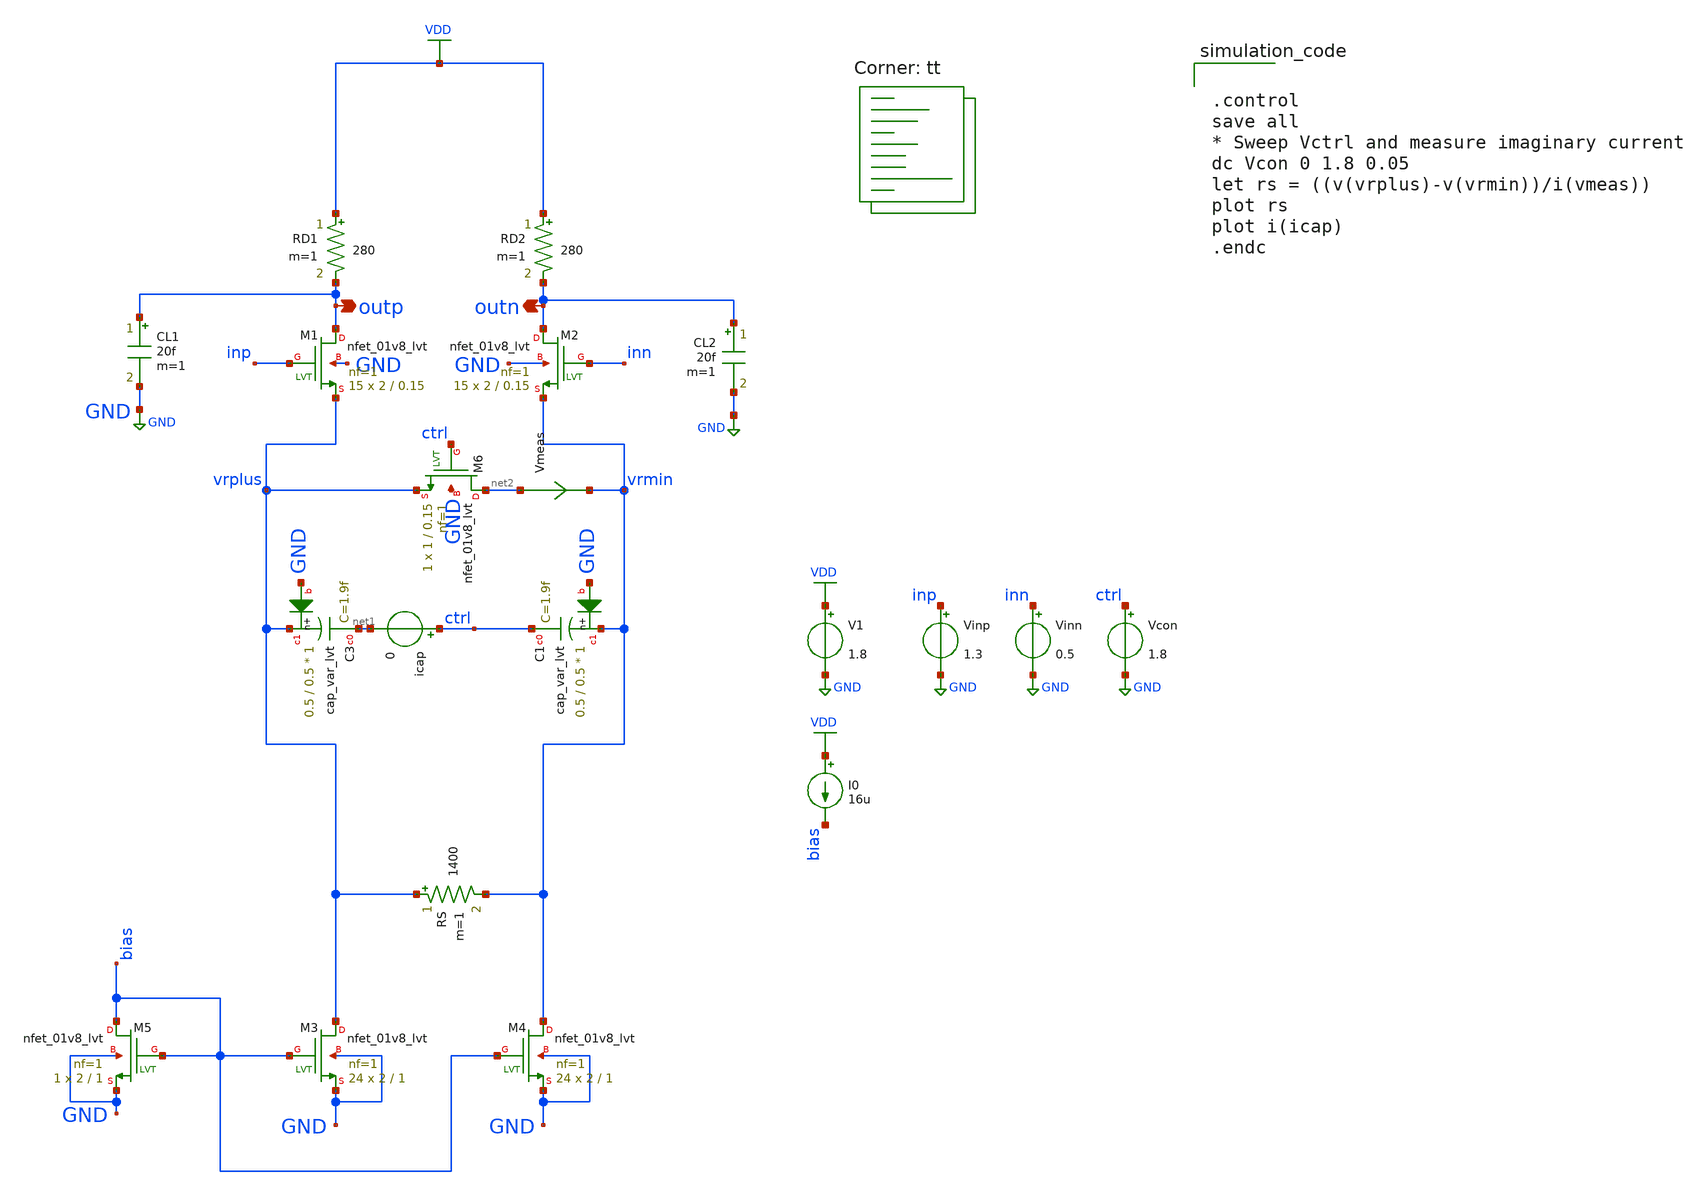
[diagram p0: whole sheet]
** sch_path: CTLE/ctle_sym_adaptive_cap.sch
**.subckt ctle_sym_adaptive_cap outp outn
*.opin outp
*.opin outn
XM1 outp inp vrplus GND sky130_fd_pr__nfet_01v8_lvt L=0.15 W=2 nf=1 ad='int((nf+1)/2) * W/nf * 0.29'
+ as='int((nf+2)/2) * W/nf * 0.29' pd='2*int((nf+1)/2) * (W/nf + 0.29)' ps='2*int((nf+2)/2) * (W/nf + 0.29)'
+ nrd='0.29 / W' nrs='0.29 / W' sa=0 sb=0 sd=0 mult=15 m=15
XM2 outn inn vrmin GND sky130_fd_pr__nfet_01v8_lvt L=0.15 W=2 nf=1 ad='int((nf+1)/2) * W/nf * 0.29' as='int((nf+2)/2) * W/nf * 0.29'
+ pd='2*int((nf+1)/2) * (W/nf + 0.29)' ps='2*int((nf+2)/2) * (W/nf + 0.29)' nrd='0.29 / W' nrs='0.29 / W'
+ sa=0 sb=0 sd=0 mult=15 m=15
XM3 vrplus bias GND GND sky130_fd_pr__nfet_01v8_lvt L=1 W=2 nf=1 ad='int((nf+1)/2) * W/nf * 0.29' as='int((nf+2)/2) * W/nf * 0.29'
+ pd='2*int((nf+1)/2) * (W/nf + 0.29)' ps='2*int((nf+2)/2) * (W/nf + 0.29)' nrd='0.29 / W' nrs='0.29 / W'
+ sa=0 sb=0 sd=0 mult=24 m=24
XM4 vrmin bias GND GND sky130_fd_pr__nfet_01v8_lvt L=1 W=2 nf=1 ad='int((nf+1)/2) * W/nf * 0.29' as='int((nf+2)/2) * W/nf * 0.29'
+ pd='2*int((nf+1)/2) * (W/nf + 0.29)' ps='2*int((nf+2)/2) * (W/nf + 0.29)' nrd='0.29 / W' nrs='0.29 / W'
+ sa=0 sb=0 sd=0 mult=24 m=24
XM5 bias bias GND GND sky130_fd_pr__nfet_01v8_lvt L=1 W=2 nf=1 ad='int((nf+1)/2) * W/nf * 0.29' as='int((nf+2)/2) * W/nf * 0.29'
+ pd='2*int((nf+1)/2) * (W/nf + 0.29)' ps='2*int((nf+2)/2) * (W/nf + 0.29)' nrd='0.29 / W' nrs='0.29 / W'
+ sa=0 sb=0 sd=0 mult=1 m=1
RD1 VDD outp 280 m=1
RD2 VDD outn 280 m=1
RS vrplus vrmin 1400 m=1
CL1 outp GND 20f m=1
CL2 outn GND 20f m=1
XM6 net2 ctrl vrplus GND sky130_fd_pr__nfet_01v8_lvt L=0.15 W=1 nf=1 ad='int((nf+1)/2) * W/nf * 0.29'
+ as='int((nf+2)/2) * W/nf * 0.29' pd='2*int((nf+1)/2) * (W/nf + 0.29)' ps='2*int((nf+2)/2) * (W/nf + 0.29)'
+ nrd='0.29 / W' nrs='0.29 / W' sa=0 sb=0 sd=0 mult=1 m=1
V1 VDD GND 1.8
Vinp inp GND 1.3
Vinn inn GND 0.5
Vcon ctrl GND 1.8
I0 VDD bias 16u
XC3 net1 vrplus GND sky130_fd_pr__cap_var_lvt W=0.5 L=0.5 VM=1 m=1
XC1 ctrl vrmin GND sky130_fd_pr__cap_var_lvt W=0.5 L=0.5 VM=1 m=1
icap ctrl net1 0
.save i(icap)
Vmeas net2 vrmin 0
.save i(vmeas)
**** begin user architecture code
.lib $::SKYWATER_MODELS/sky130.lib.spice tt


.control
save all
* Sweep Vctrl and measure imaginary current
dc Vcon 0 1.8 0.05
let rs = ((v(vrplus)-v(vrmin))/i(vmeas))
plot rs
plot i(icap)
.endc


**** end user architecture code
**.ends
.GLOBAL GND
.GLOBAL VDD
.end
